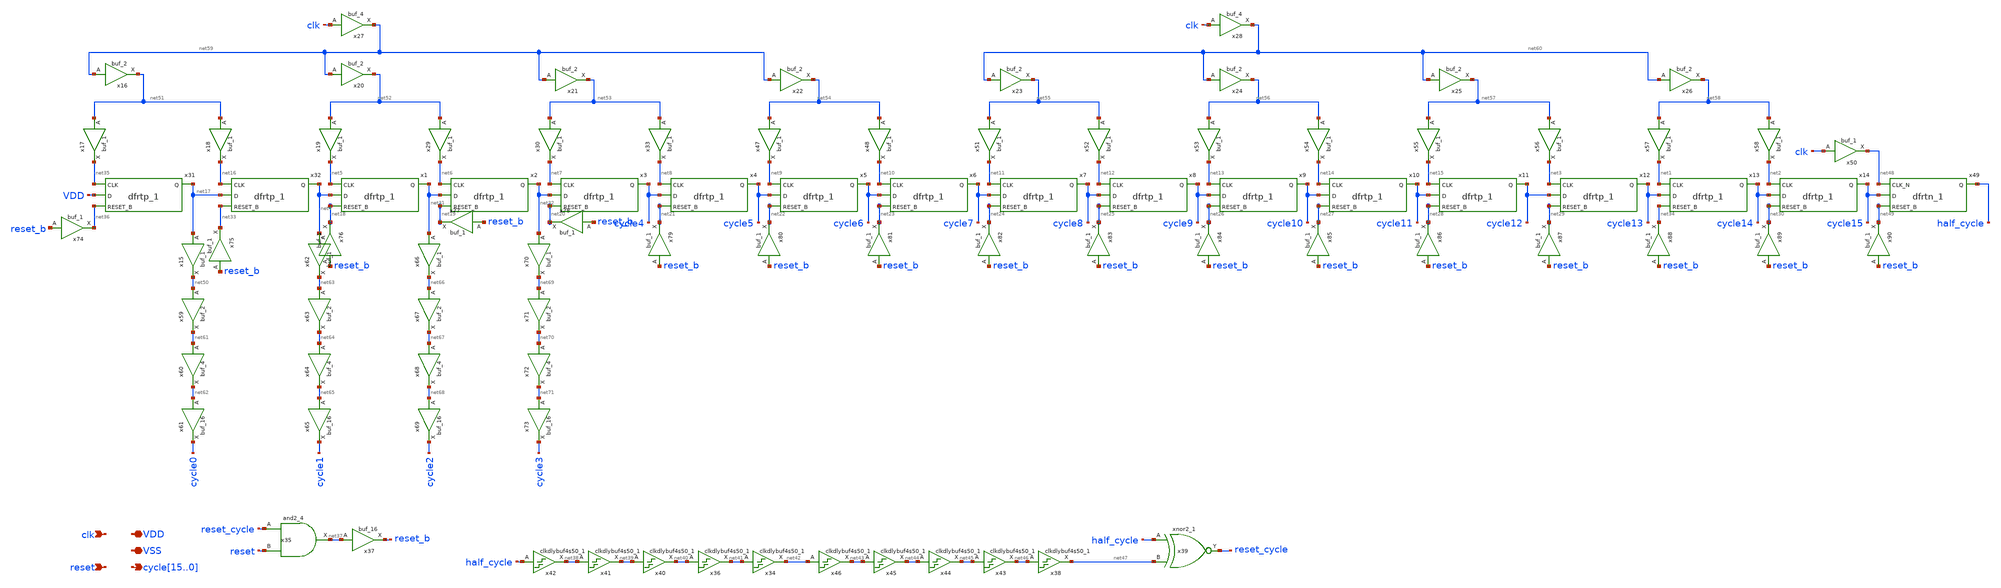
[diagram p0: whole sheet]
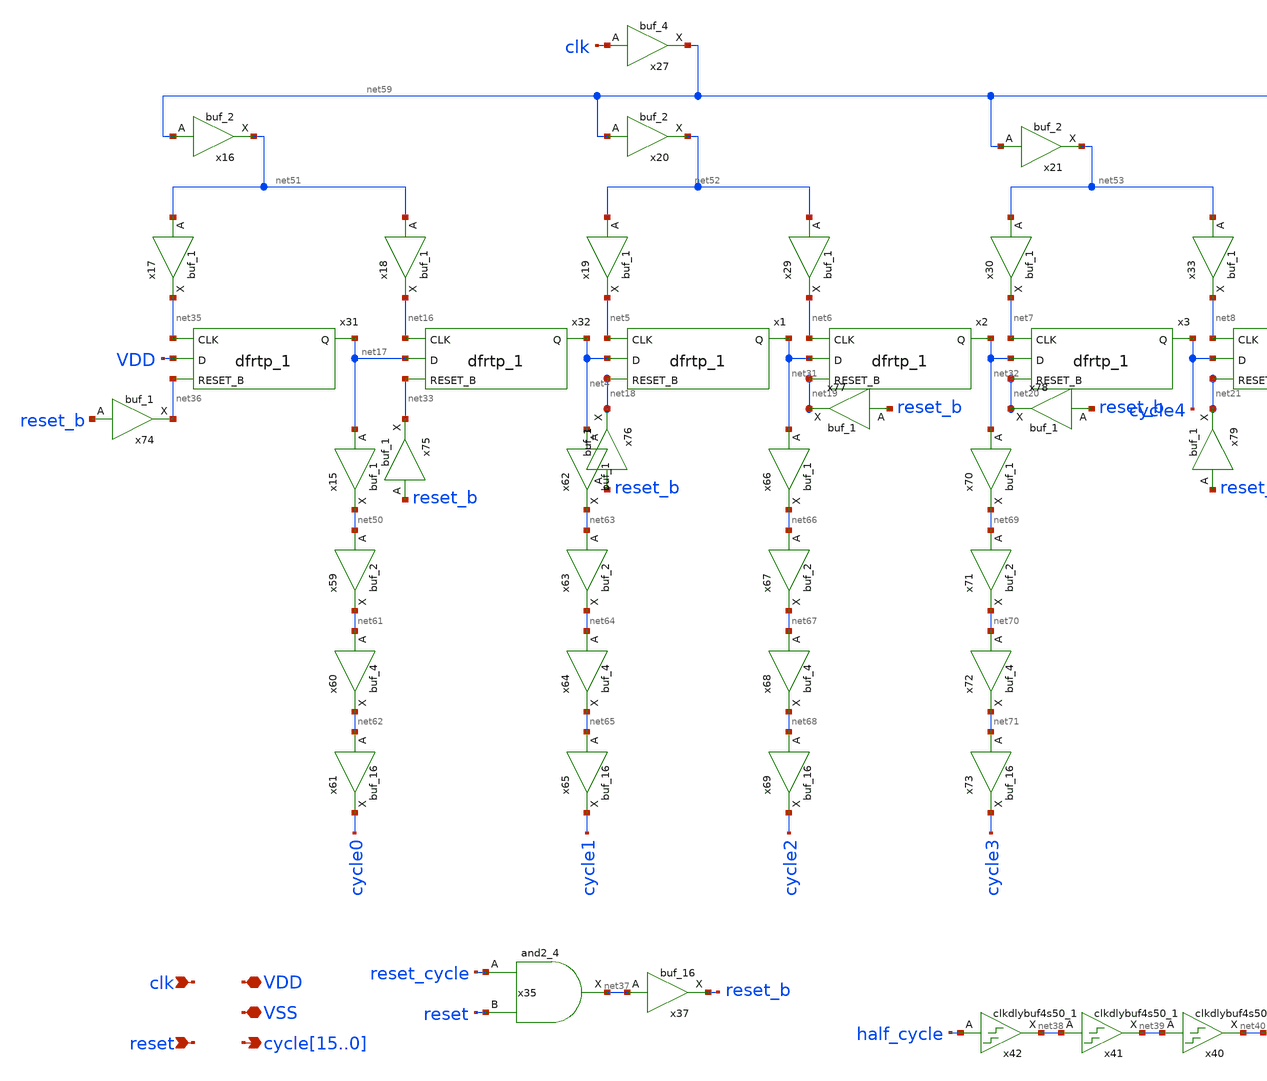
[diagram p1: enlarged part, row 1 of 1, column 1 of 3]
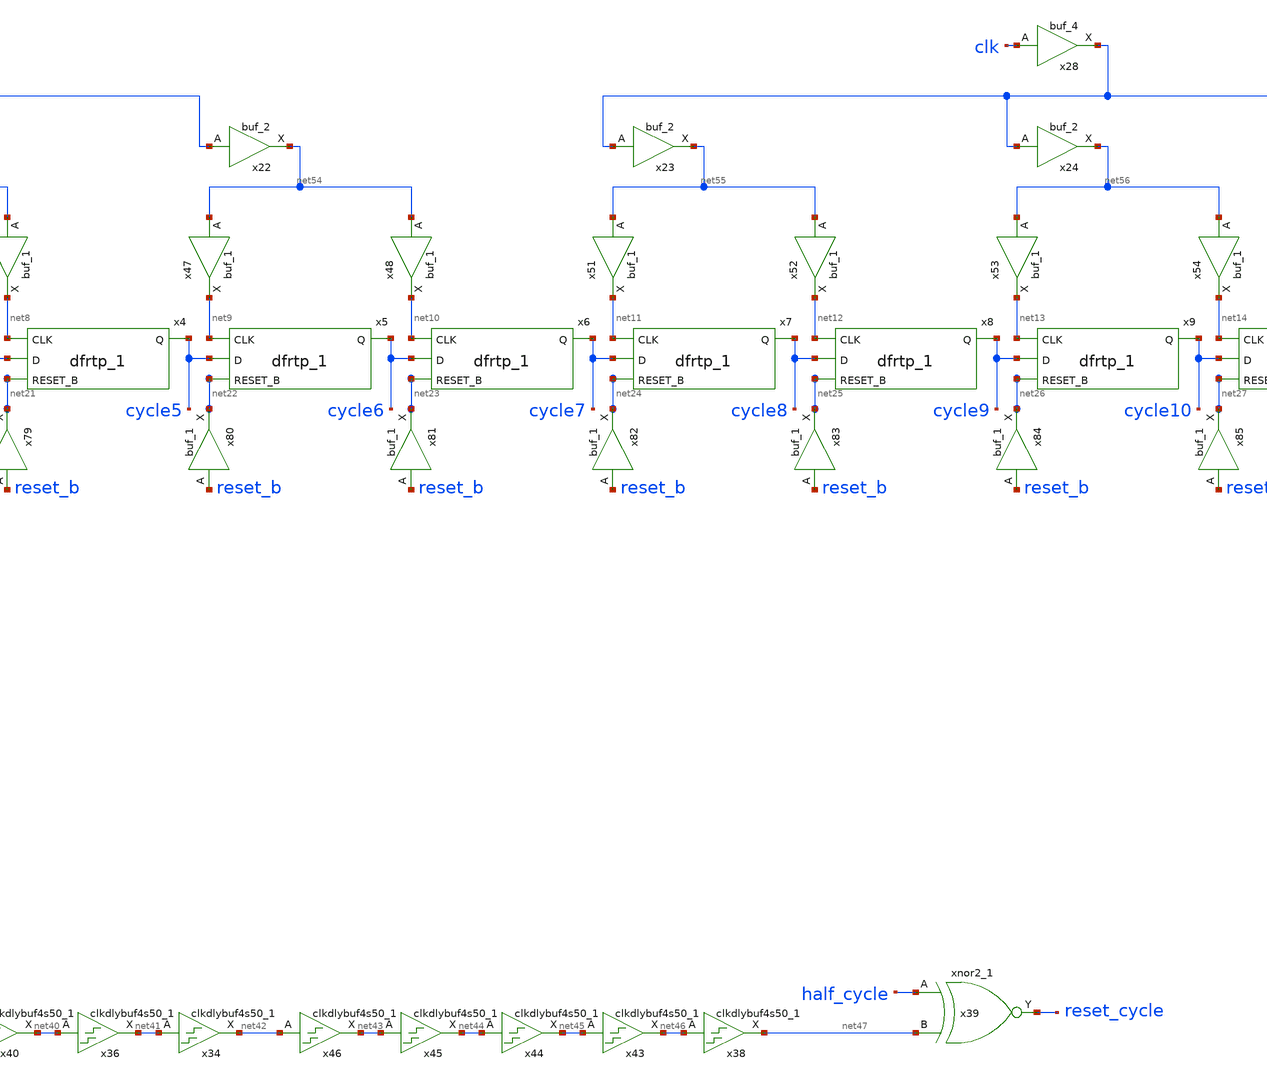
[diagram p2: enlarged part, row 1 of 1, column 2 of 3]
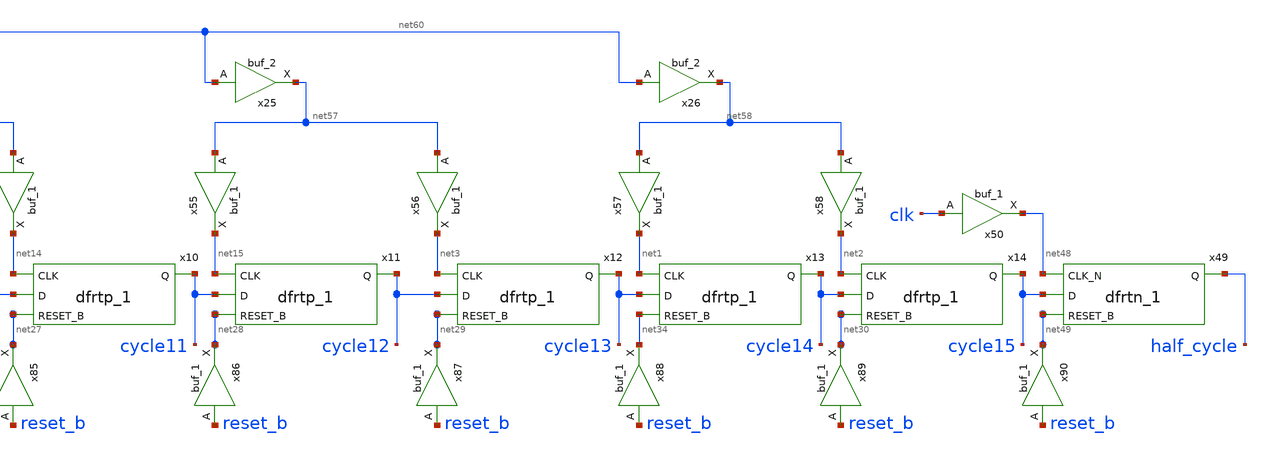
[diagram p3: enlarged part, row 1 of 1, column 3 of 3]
** sch_path: xschem/src/shifted_clock_generator/shifted_clock_generator.sch
**.subckt shifted_clock_generator
*+ cycle15,cycle14,cycle13,cycle12,cycle11,cycle10,cycle9,cycle8,cycle7,cycle6,cycle5,cycle4,cycle3,cycle2,cycle1,cycle0 VSS VDD clk reset
*.opin
*+ cycle15,cycle14,cycle13,cycle12,cycle11,cycle10,cycle9,cycle8,cycle7,cycle6,cycle5,cycle4,cycle3,cycle2,cycle1,cycle0
*.iopin VSS
*.iopin VDD
*.ipin clk
*.ipin reset
x32 net16 net17 net33 VSS VSS VDD VDD net4 sky130_fd_sc_hd__dfrtp_1
x1 net5 net4 net18 VSS VSS VDD VDD net31 sky130_fd_sc_hd__dfrtp_1
x2 net6 net31 net19 VSS VSS VDD VDD net32 sky130_fd_sc_hd__dfrtp_1
x3 net7 net32 net20 VSS VSS VDD VDD cycle4 sky130_fd_sc_hd__dfrtp_1
x4 net8 cycle4 net21 VSS VSS VDD VDD cycle5 sky130_fd_sc_hd__dfrtp_1
x5 net9 cycle5 net22 VSS VSS VDD VDD cycle6 sky130_fd_sc_hd__dfrtp_1
x6 net10 cycle6 net23 VSS VSS VDD VDD cycle7 sky130_fd_sc_hd__dfrtp_1
x7 net11 cycle7 net24 VSS VSS VDD VDD cycle8 sky130_fd_sc_hd__dfrtp_1
x8 net12 cycle8 net25 VSS VSS VDD VDD cycle9 sky130_fd_sc_hd__dfrtp_1
x9 net13 cycle9 net26 VSS VSS VDD VDD cycle10 sky130_fd_sc_hd__dfrtp_1
x10 net14 cycle10 net27 VSS VSS VDD VDD cycle11 sky130_fd_sc_hd__dfrtp_1
x11 net15 cycle11 net28 VSS VSS VDD VDD cycle12 sky130_fd_sc_hd__dfrtp_1
x12 net3 cycle12 net29 VSS VSS VDD VDD cycle13 sky130_fd_sc_hd__dfrtp_1
x13 net1 cycle13 net34 VSS VSS VDD VDD cycle14 sky130_fd_sc_hd__dfrtp_1
x14 net2 cycle14 net30 VSS VSS VDD VDD cycle15 sky130_fd_sc_hd__dfrtp_1
x31 net35 VDD net36 VSS VSS VDD VDD net17 sky130_fd_sc_hd__dfrtp_1
x37 net37 VSS VSS VDD VDD reset_b sky130_fd_sc_hd__buf_16
x35 reset_cycle reset VSS VSS VDD VDD net37 sky130_fd_sc_hd__and2_4
x34 net41 VSS VSS VDD VDD net42 sky130_fd_sc_hd__clkdlybuf4s50_1
x39 half_cycle net47 VSS VSS VDD VDD reset_cycle sky130_fd_sc_hd__xnor2_1
x36 net40 VSS VSS VDD VDD net41 sky130_fd_sc_hd__clkdlybuf4s50_1
x40 net39 VSS VSS VDD VDD net40 sky130_fd_sc_hd__clkdlybuf4s50_1
x41 net38 VSS VSS VDD VDD net39 sky130_fd_sc_hd__clkdlybuf4s50_1
x42 half_cycle VSS VSS VDD VDD net38 sky130_fd_sc_hd__clkdlybuf4s50_1
x38 net46 VSS VSS VDD VDD net47 sky130_fd_sc_hd__clkdlybuf4s50_1
x43 net45 VSS VSS VDD VDD net46 sky130_fd_sc_hd__clkdlybuf4s50_1
x44 net44 VSS VSS VDD VDD net45 sky130_fd_sc_hd__clkdlybuf4s50_1
x45 net43 VSS VSS VDD VDD net44 sky130_fd_sc_hd__clkdlybuf4s50_1
x46 net42 VSS VSS VDD VDD net43 sky130_fd_sc_hd__clkdlybuf4s50_1
x49 net48 cycle15 net49 VSS VSS VDD VDD half_cycle sky130_fd_sc_hd__dfrtn_1
x50 clk VSS VSS VDD VDD net48 sky130_fd_sc_hd__buf_1
x15 net17 VSS VSS VDD VDD net50 sky130_fd_sc_hd__buf_1
x16 net59 VSS VSS VDD VDD net51 sky130_fd_sc_hd__buf_2
x20 net59 VSS VSS VDD VDD net52 sky130_fd_sc_hd__buf_2
x21 net59 VSS VSS VDD VDD net53 sky130_fd_sc_hd__buf_2
x22 net59 VSS VSS VDD VDD net54 sky130_fd_sc_hd__buf_2
x23 net60 VSS VSS VDD VDD net55 sky130_fd_sc_hd__buf_2
x24 net60 VSS VSS VDD VDD net56 sky130_fd_sc_hd__buf_2
x25 net60 VSS VSS VDD VDD net57 sky130_fd_sc_hd__buf_2
x26 net60 VSS VSS VDD VDD net58 sky130_fd_sc_hd__buf_2
x27 clk VSS VSS VDD VDD net59 sky130_fd_sc_hd__buf_4
x28 clk VSS VSS VDD VDD net60 sky130_fd_sc_hd__buf_4
x17 net51 VSS VSS VDD VDD net35 sky130_fd_sc_hd__buf_1
x18 net51 VSS VSS VDD VDD net16 sky130_fd_sc_hd__buf_1
x19 net52 VSS VSS VDD VDD net5 sky130_fd_sc_hd__buf_1
x29 net52 VSS VSS VDD VDD net6 sky130_fd_sc_hd__buf_1
x30 net53 VSS VSS VDD VDD net7 sky130_fd_sc_hd__buf_1
x33 net53 VSS VSS VDD VDD net8 sky130_fd_sc_hd__buf_1
x47 net54 VSS VSS VDD VDD net9 sky130_fd_sc_hd__buf_1
x48 net54 VSS VSS VDD VDD net10 sky130_fd_sc_hd__buf_1
x51 net55 VSS VSS VDD VDD net11 sky130_fd_sc_hd__buf_1
x52 net55 VSS VSS VDD VDD net12 sky130_fd_sc_hd__buf_1
x53 net56 VSS VSS VDD VDD net13 sky130_fd_sc_hd__buf_1
x54 net56 VSS VSS VDD VDD net14 sky130_fd_sc_hd__buf_1
x55 net57 VSS VSS VDD VDD net15 sky130_fd_sc_hd__buf_1
x56 net57 VSS VSS VDD VDD net3 sky130_fd_sc_hd__buf_1
x57 net58 VSS VSS VDD VDD net1 sky130_fd_sc_hd__buf_1
x58 net58 VSS VSS VDD VDD net2 sky130_fd_sc_hd__buf_1
x59 net50 VSS VSS VDD VDD net61 sky130_fd_sc_hd__buf_2
x60 net61 VSS VSS VDD VDD net62 sky130_fd_sc_hd__buf_4
x61 net62 VSS VSS VDD VDD cycle0 sky130_fd_sc_hd__buf_16
x62 net4 VSS VSS VDD VDD net63 sky130_fd_sc_hd__buf_1
x63 net63 VSS VSS VDD VDD net64 sky130_fd_sc_hd__buf_2
x64 net64 VSS VSS VDD VDD net65 sky130_fd_sc_hd__buf_4
x65 net65 VSS VSS VDD VDD cycle1 sky130_fd_sc_hd__buf_16
x66 net31 VSS VSS VDD VDD net66 sky130_fd_sc_hd__buf_1
x67 net66 VSS VSS VDD VDD net67 sky130_fd_sc_hd__buf_2
x68 net67 VSS VSS VDD VDD net68 sky130_fd_sc_hd__buf_4
x69 net68 VSS VSS VDD VDD cycle2 sky130_fd_sc_hd__buf_16
x70 net32 VSS VSS VDD VDD net69 sky130_fd_sc_hd__buf_1
x71 net69 VSS VSS VDD VDD net70 sky130_fd_sc_hd__buf_2
x72 net70 VSS VSS VDD VDD net71 sky130_fd_sc_hd__buf_4
x73 net71 VSS VSS VDD VDD cycle3 sky130_fd_sc_hd__buf_16
x74 reset_b VSS VSS VDD VDD net36 sky130_fd_sc_hd__buf_1
x75 reset_b VSS VSS VDD VDD net33 sky130_fd_sc_hd__buf_1
x76 reset_b VSS VSS VDD VDD net18 sky130_fd_sc_hd__buf_1
x77 reset_b VSS VSS VDD VDD net19 sky130_fd_sc_hd__buf_1
x78 reset_b VSS VSS VDD VDD net20 sky130_fd_sc_hd__buf_1
x79 reset_b VSS VSS VDD VDD net21 sky130_fd_sc_hd__buf_1
x80 reset_b VSS VSS VDD VDD net22 sky130_fd_sc_hd__buf_1
x81 reset_b VSS VSS VDD VDD net23 sky130_fd_sc_hd__buf_1
x82 reset_b VSS VSS VDD VDD net24 sky130_fd_sc_hd__buf_1
x83 reset_b VSS VSS VDD VDD net25 sky130_fd_sc_hd__buf_1
x84 reset_b VSS VSS VDD VDD net26 sky130_fd_sc_hd__buf_1
x85 reset_b VSS VSS VDD VDD net27 sky130_fd_sc_hd__buf_1
x86 reset_b VSS VSS VDD VDD net28 sky130_fd_sc_hd__buf_1
x87 reset_b VSS VSS VDD VDD net29 sky130_fd_sc_hd__buf_1
x88 reset_b VSS VSS VDD VDD net34 sky130_fd_sc_hd__buf_1
x89 reset_b VSS VSS VDD VDD net30 sky130_fd_sc_hd__buf_1
x90 reset_b VSS VSS VDD VDD net49 sky130_fd_sc_hd__buf_1
**.ends
.end
